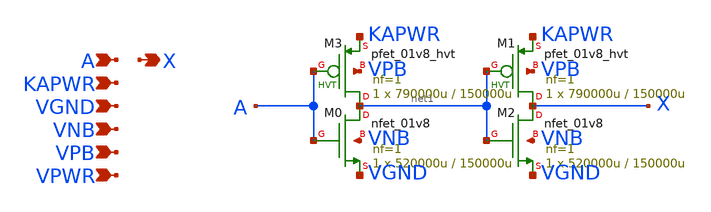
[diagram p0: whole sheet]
** sch_path: schematics/lpflow_clkbufkapwr/sky130_fd_sc_hd__lpflow_clkbufkapwr_1.sch
**.subckt sky130_fd_sc_hd__lpflow_clkbufkapwr_1 A KAPWR VGND VNB VPB VPWR X
*.ipin A
*.ipin KAPWR
*.ipin VGND
*.ipin VNB
*.ipin VPB
*.ipin VPWR
*.opin X
XM3 net1 A KAPWR VPB sky130_fd_pr__pfet_01v8_hvt L=150000u W=790000u nf=1 ad='int((1 + 1)/2) * 790000u / 1 * 0.29'
+ as='int((1 + 2)/2) * 790000u / 1 * 0.29' pd='2*int((1 + 1)/2) * (790000u / 1 + 0.29)' ps='2*int((1 + 2)/2) * (790000u / 1 + 0.29)'
+ nrd='0.29 / 790000u ' nrs='0.29 / 790000u ' sa=0 sb=0 sd=0 mult=1 m=1
XM1 X net1 KAPWR VPB sky130_fd_pr__pfet_01v8_hvt L=150000u W=790000u nf=1 ad='int((1 + 1)/2) * 790000u / 1 * 0.29'
+ as='int((1 + 2)/2) * 790000u / 1 * 0.29' pd='2*int((1 + 1)/2) * (790000u / 1 + 0.29)' ps='2*int((1 + 2)/2) * (790000u / 1 + 0.29)'
+ nrd='0.29 / 790000u ' nrs='0.29 / 790000u ' sa=0 sb=0 sd=0 mult=1 m=1
XM0 net1 A VGND VNB sky130_fd_pr__nfet_01v8 L=150000u W=520000u nf=1 ad='int((1 + 1)/2) * 520000u / 1 * 0.29'
+ as='int((1 + 2)/2) * 520000u / 1 * 0.29' pd='2*int((1 + 1)/2) * (520000u / 1 + 0.29)' ps='2*int((1 + 2)/2) * (520000u / 1 + 0.29)'
+ nrd='0.29 / 520000u ' nrs='0.29 / 520000u ' sa=0 sb=0 sd=0 mult=1 m=1
XM2 X net1 VGND VNB sky130_fd_pr__nfet_01v8 L=150000u W=520000u nf=1 ad='int((1 + 1)/2) * 520000u / 1 * 0.29'
+ as='int((1 + 2)/2) * 520000u / 1 * 0.29' pd='2*int((1 + 1)/2) * (520000u / 1 + 0.29)' ps='2*int((1 + 2)/2) * (520000u / 1 + 0.29)'
+ nrd='0.29 / 520000u ' nrs='0.29 / 520000u ' sa=0 sb=0 sd=0 mult=1 m=1
**.ends
.end
